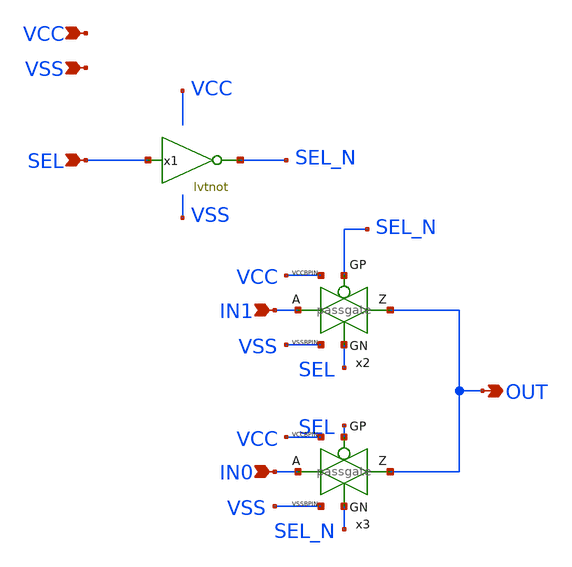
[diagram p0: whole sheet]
** sch_path: xschem/onehot2mux.sch
**.subckt onehot2mux SEL IN0 IN1 OUT VCC VSS
*.ipin SEL
*.ipin IN0
*.ipin IN1
*.opin OUT
*.ipin VCC
*.ipin VSS
x2 OUT IN1 SEL_N SEL VCC passgate
x3 OUT IN0 SEL SEL_N VCC passgate
x1 SEL SEL_N VCC VSS lvtnot W_N=1 L_N=0.15 W_P=2 L_P=0.35 m=1
**.ends
.end
